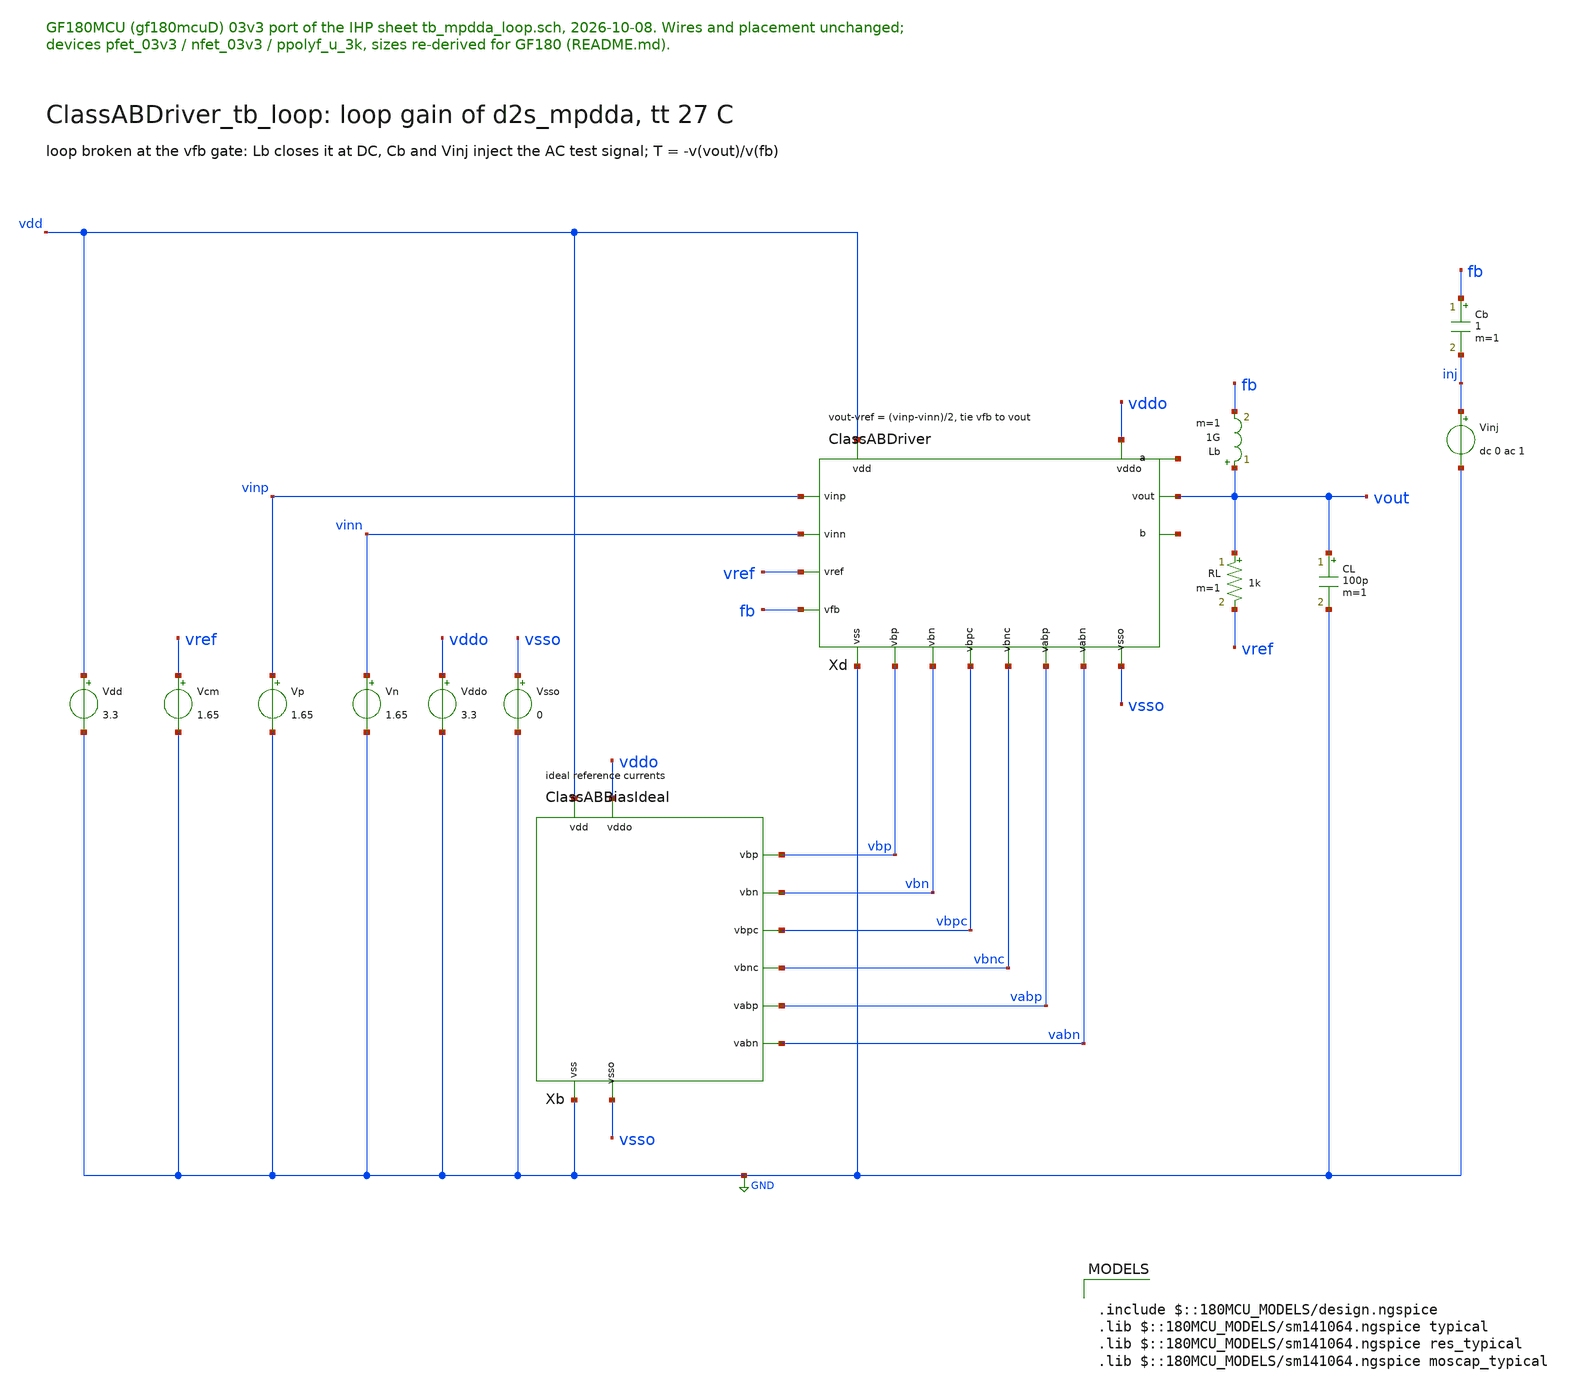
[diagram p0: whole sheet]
** sch_path: macros/ClassABDriver/testbenches/xschem/ClassABDriver_tb_loop.sch
**.subckt ClassABDriver_tb_loop
Vdd vdd GND 3.3
Vcm vref GND 1.65
Xb vdd GND vddo vsso vbp vbn vbpc vbnc vabp vabn ClassABBiasIdeal
Xd vdd GND vddo vsso vinp vinn vref vout fb vbp vbn vbpc vbnc vabp vabn net1 net2 ClassABDriver
Vp vinp GND 1.65
Vn vinn GND 1.65
RL vout vref 1k m=1
CL vout GND 100p m=1
Lb vout fb 1G m=1
Cb fb inj 1 m=1
Vinj inj GND dc 0 ac 1
Vddo vddo GND 3.3
Vsso vsso GND 0
**** begin user architecture code

.control
ac dec 50 10 1G
let T=-v(vout)/v(fb)
meas ac T0 find vdb(T) at=10
meas ac fc when vdb(T)=0
meas ac pT find vp(T) when vdb(T)=0
let pm=180/pi*pT+180
print T0 fc pm
if $?batchmode = 0
  plot vdb(T) 180/pi*vp(T)
end
.endc


.include $::180MCU_MODELS/design.ngspice
.lib $::180MCU_MODELS/sm141064.ngspice typical
.lib $::180MCU_MODELS/sm141064.ngspice res_typical
.lib $::180MCU_MODELS/sm141064.ngspice moscap_typical

**** end user architecture code
**.ends
.GLOBAL GND
.end
